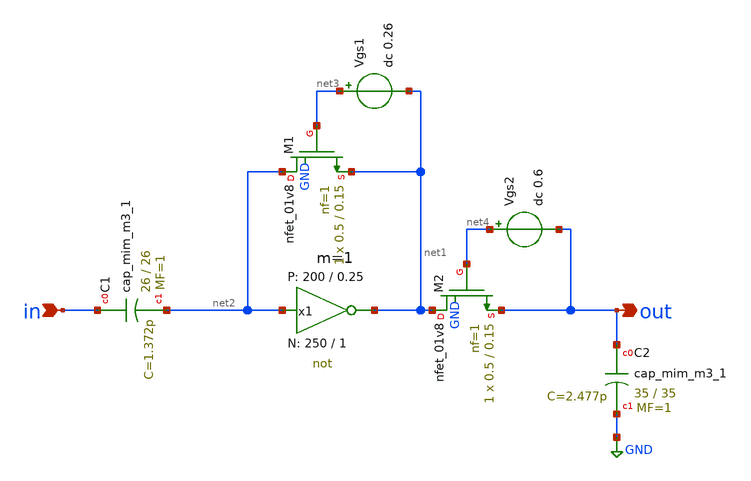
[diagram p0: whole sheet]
** sch_path: Amplifier_Inv/xschem/v2/inv_sky130_a_v2.sch
* StefanSchippers/xschem_sky130/sky130_tests/not.sch:
* Copyright 2021 Stefan Frederik Schippers
* Licensed under the Apache License, Version 2.0 (the "License");
**.subckt inv_sky130_a_v2 in out
*.ipin in
*.opin out
x1 net1 net2 VCC VSS not W_N=250 L_N=1 W_P=200 L_P=0.25 m=1
XC2 out GND sky130_fd_pr__cap_mim_m3_1 W=35 L=35 MF=1 m=1
XC1 in net2 sky130_fd_pr__cap_mim_m3_1 W=26 L=26 MF=1 m=1
XM1 net2 net3 net1 GND sky130_fd_pr__nfet_01v8 L=0.15 W=0.5 nf=1 ad='int((nf+1)/2) * W/nf * 0.29' as='int((nf+2)/2) * W/nf * 0.29'
+ pd='2*int((nf+1)/2) * (W/nf + 0.29)' ps='2*int((nf+2)/2) * (W/nf + 0.29)' nrd='0.29 / W' nrs='0.29 / W'
+ sa=0 sb=0 sd=0 mult=1 m=1
Vgs1 net3 net1 dc 0.26
XM2 net1 net4 out GND sky130_fd_pr__nfet_01v8 L=0.15 W=0.5 nf=1 ad='int((nf+1)/2) * W/nf * 0.29' as='int((nf+2)/2) * W/nf * 0.29'
+ pd='2*int((nf+1)/2) * (W/nf + 0.29)' ps='2*int((nf+2)/2) * (W/nf + 0.29)' nrd='0.29 / W' nrs='0.29 / W'
+ sa=0 sb=0 sd=0 mult=1 m=1
Vgs2 net4 out dc 0.6
**.ends

* expanding   symbol:  sky130_tests/not.sym # of pins=2
** sym_path: sky130_tests/not.sym
** sch_path: sky130_tests/not.sch
.subckt not y a VCCPIN VSSPIN     W_N=1 L_N=0.15 W_P=2 L_P=0.15
*.opin y
*.ipin a
XM1 DN a VSSPIN VSSPIN sky130_fd_pr__nfet_01v8 L=L_N W=W_N nf=1 ad='int((1 + 1)/2) * W_N / 1 * 0.29'
+ as='int((1 + 2)/2) * W_N / 1 * 0.29' pd='2*int((1 + 1)/2) * (W_N / 1 + 0.29)' ps='2*int((1 + 2)/2) * (W_N / 1 + 0.29)'
+ nrd='0.29 / W_N ' nrs='0.29 / W_N ' sa=0 sb=0 sd=0 mult=1 m=1
XM2 DP a VCCPIN VCCPIN sky130_fd_pr__pfet_01v8 L=L_P W=W_P nf=1 ad='int((nf+1)/2) * W/nf * 0.29' as='int((nf+2)/2) * W/nf * 0.29'
+ pd='2*int((nf+1)/2) * (W/nf + 0.29)' ps='2*int((nf+2)/2) * (W/nf + 0.29)' nrd='0.29 / W' nrs='0.29 / W'
+ sa=0 sb=0 sd=0 mult=1 m=1
Vmeas DP y 0
.save i(vmeas)
Vmeas1 y DN 0
.save i(vmeas1)
.save v(dp)
.save v(dn)
.ends

.GLOBAL GND
.end
